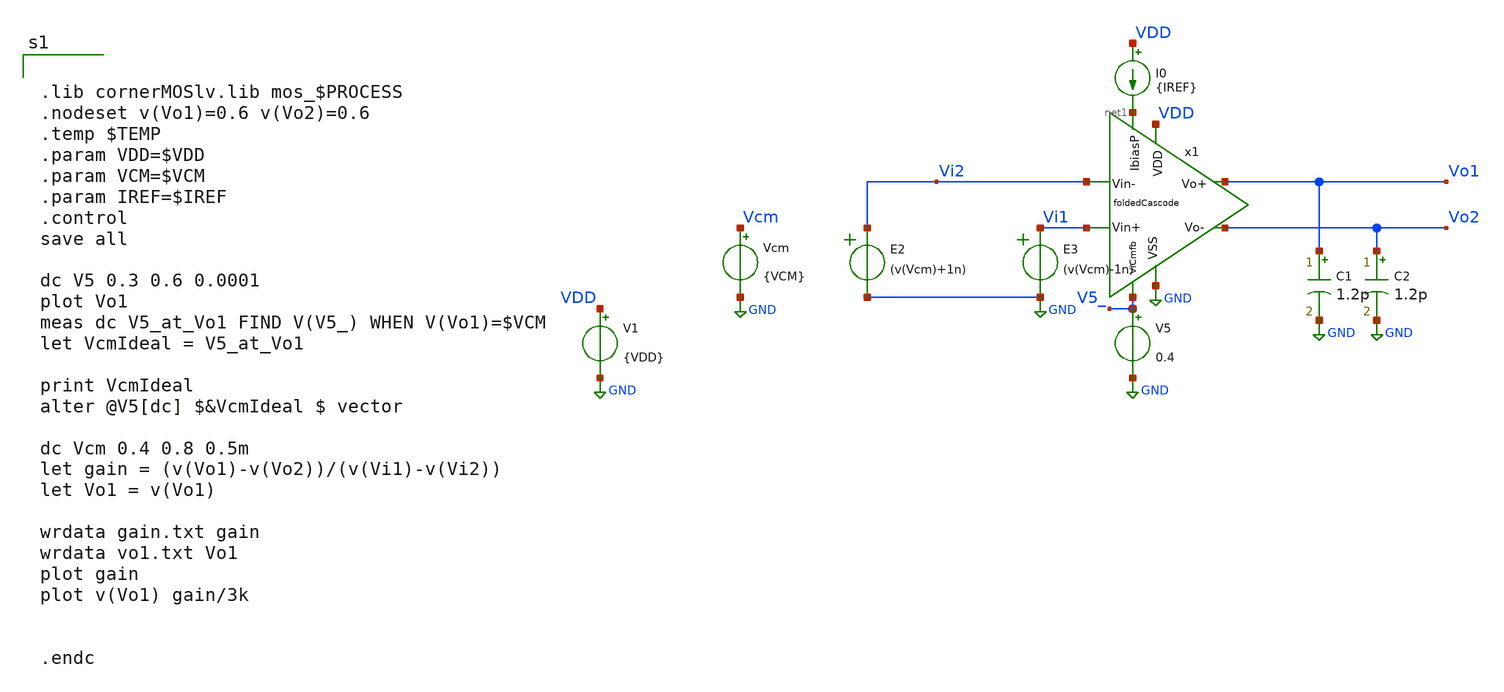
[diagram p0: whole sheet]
** sch_path: sch/AutoTestbench/tb/done/icmr.sch
**.subckt icmr
x1 VDD GND V5_ net1 Vo1 Vo2 Vi2 Vi1 foldedCascode
V1 VDD GND {VDD}
I0 VDD net1 {IREF}
C1 Vo1 GND 1.2p m=1
C2 Vo2 GND 1.2p m=1
V5 V5_ GND 0.4
Vcm Vcm GND {VCM}
E2 Vi2 GND VOL=' (v(Vcm)+1n) '
E3 Vi1 GND VOL=' (v(Vcm)-1n) '
**** begin user architecture code


.lib cornerMOSlv.lib mos_$PROCESS
.nodeset v(Vo1)=0.6 v(Vo2)=0.6
.temp $TEMP
.param VDD=$VDD
.param VCM=$VCM
.param IREF=$IREF
.control
save all

dc V5 0.3 0.6 0.0001
plot Vo1
meas dc V5_at_Vo1 FIND V(V5_) WHEN V(Vo1)=$VCM
let VcmIdeal = V5_at_Vo1

print VcmIdeal
alter @V5[dc] $&VcmIdeal $ vector

dc Vcm 0.4 0.8 0.5m
let gain = (v(Vo1)-v(Vo2))/(v(Vi1)-v(Vi2))
let Vo1 = v(Vo1)

wrdata gain.txt gain
wrdata vo1.txt Vo1
plot gain
plot v(Vo1) gain/3k


.endc


**** end user architecture code
**.ends

* expanding   symbol:  foldedCascode.sym # of pins=8
** sym_path: sch/blocks/foldedCascode.sym
** sch_path: sch/blocks/foldedCascode.sch
.subckt foldedCascode VDD VSS ViCmfb IbiasP Vo+ Vo- Vin- Vin+
*.iopin VSS
*.iopin VDD
*.ipin ViCmfb
*.iopin IbiasP
*.ipin Vin+
*.ipin Vin-
*.iopin Vo+
*.iopin Vo-
x1 VDD Vb1_1 Vb1_2 Vx Vy VSS IbiasN gmBoosting
XM1 Vy Vin+ net3 net3 sg13_lv_pmos w=115u l=0.13u ng=100 m=2 mm_ok=1
XM2 Vx Vin- net3 net3 sg13_lv_pmos w=115u l=0.13u ng=100 m=2 mm_ok=1
XM3 Vo+ Vb1_1 Vx VSS sg13_lv_nmos w=44.4u l=0.3u ng=22 m=6 mm_ok=1
XM12 Vx ViCmfb VSS VSS sg13_lv_nmos w=24.3u l=0.8u ng=62 m=6 mm_ok=1
XM4 Vo- Vb1_2 Vy VSS sg13_lv_nmos w=44.4u l=0.3u ng=22 m=6 mm_ok=1
XM5 Vy ViCmfb VSS VSS sg13_lv_nmos w=24.3u l=0.8u ng=62 m=6 mm_ok=1
XM6 Vb0 Vb0 net4 VDD sg13_lv_pmos w=65u l=0.13u ng=65 m=1 mm_ok=1
XM13 net4 Vb0 VDD VDD sg13_lv_pmos w=26u l=0.3u ng=5 m=1 mm_ok=1
XM20 Vb3 Vb2 net6 VDD sg13_lv_pmos w=5.6u l=0.4u ng=1 m=1 mm_ok=1
XM21 net6 Vb3 VDD VDD sg13_lv_pmos w=9.7u l=0.8u ng=2 m=1 mm_ok=1
XM14 IbiasP IbiasP VSS VSS sg13_lv_nmos w=2u l=1u ng=2 m=10 mm_ok=1
XM11 Vb0 IbiasP VSS VSS sg13_lv_nmos w=2u l=1u ng=2 m=2 mm_ok=1
XM15 Vb3 IbiasP VSS VSS sg13_lv_nmos w=2u l=1u ng=2 m=2 mm_ok=1
XM16 Vb2 IbiasP VSS VSS sg13_lv_nmos w=2u l=1u ng=2 m=5 mm_ok=1
XM22 IbiasN IbiasP VSS VSS sg13_lv_nmos w=1.8u l=1u ng=2 m=10 mm_ok=1
XM23 net1 Vb3 VDD VDD sg13_lv_pmos w=63.2u l=0.8u ng=103 m=4 mm_ok=1
XM9 net2 Vb3 VDD VDD sg13_lv_pmos w=63.2u l=0.8u ng=103 m=4 mm_ok=1
XM10 Vo+ Vb2 net1 VDD sg13_lv_pmos w=100u l=0.4u ng=150 m=4 mm_ok=1
XM7 Vo- Vb2 net2 VDD sg13_lv_pmos w=100u l=0.4u ng=150 m=4 mm_ok=1
XM8 net5 Vb2 VDD VDD sg13_lv_pmos w=5.8u l=0.7u ng=1 m=1 mm_ok=1
XM17 Vb2 Vb2 net5 VDD sg13_lv_pmos w=27u l=0.4u ng=9 m=1 mm_ok=1
XM0 net3 Vb0 VDD VDD sg13_lv_pmos w=113.5u l=0.3u ng=210 m=8 mm_ok=1
.ends


* expanding   symbol:  gmBoosting.sym # of pins=7
** sym_path: sch/blocks/gmBoosting.sym
** sch_path: sch/blocks/gmBoosting.sch
.subckt gmBoosting VDD Vo2 Vo1 Vi+ Vi- VSS IbiasN
*.iopin VSS
*.opin Vo1
*.opin Vo2
*.ipin Vi+
*.ipin Vi-
*.iopin VDD
*.ipin IbiasN
XM7 net2 Vb4 VDD VDD sg13_lv_pmos w=19.8u l=0.7u ng=20 m=2 mm_ok=1
XM1 net7 Vi+ net1 net1 sg13_lv_pmos w=35u l=0.15u ng=70 m=4 mm_ok=1
XM2 net4 Vi- net1 net1 sg13_lv_pmos w=35u l=0.15u ng=70 m=4 mm_ok=1
XM0 net1 Vb0 net5 VDD sg13_lv_pmos w=12u l=0.3u ng=12 m=1 mm_ok=1
XM6 net7 Vb3 VSS VSS sg13_lv_nmos w=20.2u l=0.7u ng=5 m=2 mm_ok=1
XM9 Vo1 Vb2 net2 VDD sg13_lv_pmos w=23.2u l=0.3u ng=10 m=1 mm_ok=1
XM10 Vo2 Vb2 net3 VDD sg13_lv_pmos w=23.2u l=0.3u ng=10 m=1 mm_ok=1
XM3 net5 Vo2 VDD VDD sg13_lv_pmos w=20u l=0.13u ng=5 m=1 mm_ok=1
XM4 net5 Vo1 VDD VDD sg13_lv_pmos w=20u l=0.13u ng=5 m=1 mm_ok=1
XM5 net6 Va VDD VDD sg13_lv_pmos w=20u l=0.13u ng=5 m=2 mm_ok=1
XM29 Vb3 Vb3 VSS VSS sg13_lv_nmos w=32u l=0.7u ng=4 m=1 mm_ok=1
XM30 Vb3 Vb0 net6 VDD sg13_lv_pmos w=12u l=0.3u ng=12 m=1 mm_ok=1
XM31 net4 Vb3 VSS VSS sg13_lv_nmos w=20.2u l=0.7u ng=5 m=2 mm_ok=1
XM32 Vo1 Vb1 net4 VSS sg13_lv_nmos w=38.7u l=0.6u ng=5 m=1 mm_ok=1
XM21 IbiasN IbiasN VDD VDD sg13_lv_pmos w=18u l=1u ng=18 m=1 mm_ok=1
XM24 VbbN IbiasN VDD VDD sg13_lv_pmos w=18u l=1u ng=18 m=1 mm_ok=1
XM25 VbbN VbbN VSS VSS sg13_lv_nmos w=15u l=1u ng=2 m=1 mm_ok=1
XM17 Va VbbN VSS VSS sg13_lv_nmos w=15u l=1u ng=2 m=1 mm_ok=1
XM18 Va Va VDD VDD sg13_lv_pmos w=13u l=1u ng=13 m=1 mm_ok=1
XM19 Vb1 Vb1 net9 VSS sg13_lv_nmos w=13u l=0.7u ng=2 m=1 mm_ok=1
XM20 net9 Vb1 VSS VSS sg13_lv_nmos w=2.4u l=0.7u ng=1 m=1 mm_ok=1
XM22 Vb1 IbiasN VDD VDD sg13_lv_pmos w=18u l=1u ng=18 m=1 mm_ok=1
XM26 Vb4 Vb2 net8 VDD sg13_lv_pmos w=9u l=0.3u ng=9 m=1 mm_ok=1
XM38 net8 Vb4 VDD VDD sg13_lv_pmos w=15.5u l=0.7u ng=15 m=1 mm_ok=1
XM39 Vb4 VbbN VSS VSS sg13_lv_nmos w=15u l=1u ng=2 m=1 mm_ok=1
XM40 net11 Vb2 VDD VDD sg13_lv_pmos w=4.5u l=0.7u ng=1 m=1 mm_ok=1
XM41 Vb2 Vb2 net11 VDD sg13_lv_pmos w=15u l=0.7u ng=15 m=1 mm_ok=1
XM42 Vb2 VbbN VSS VSS sg13_lv_nmos w=15u l=1u ng=2 m=1 mm_ok=1
XM8 net3 Vb4 VDD VDD sg13_lv_pmos w=19.8u l=0.7u ng=20 m=2 mm_ok=1
XM11 Vo2 Vb1 net7 VSS sg13_lv_nmos w=38.7u l=0.6u ng=5 m=1 mm_ok=1
XM12 Vb0 VbbN VSS VSS sg13_lv_nmos w=15u l=1u ng=2 m=1 mm_ok=1
XM13 net10 Vb0 VDD VDD sg13_lv_pmos w=3.92u l=0.7u ng=2 m=1 mm_ok=1
XM14 Vb0 Vb0 net10 VDD sg13_lv_pmos w=55u l=0.15u ng=55 m=1 mm_ok=1
.ends

.GLOBAL GND
.end
